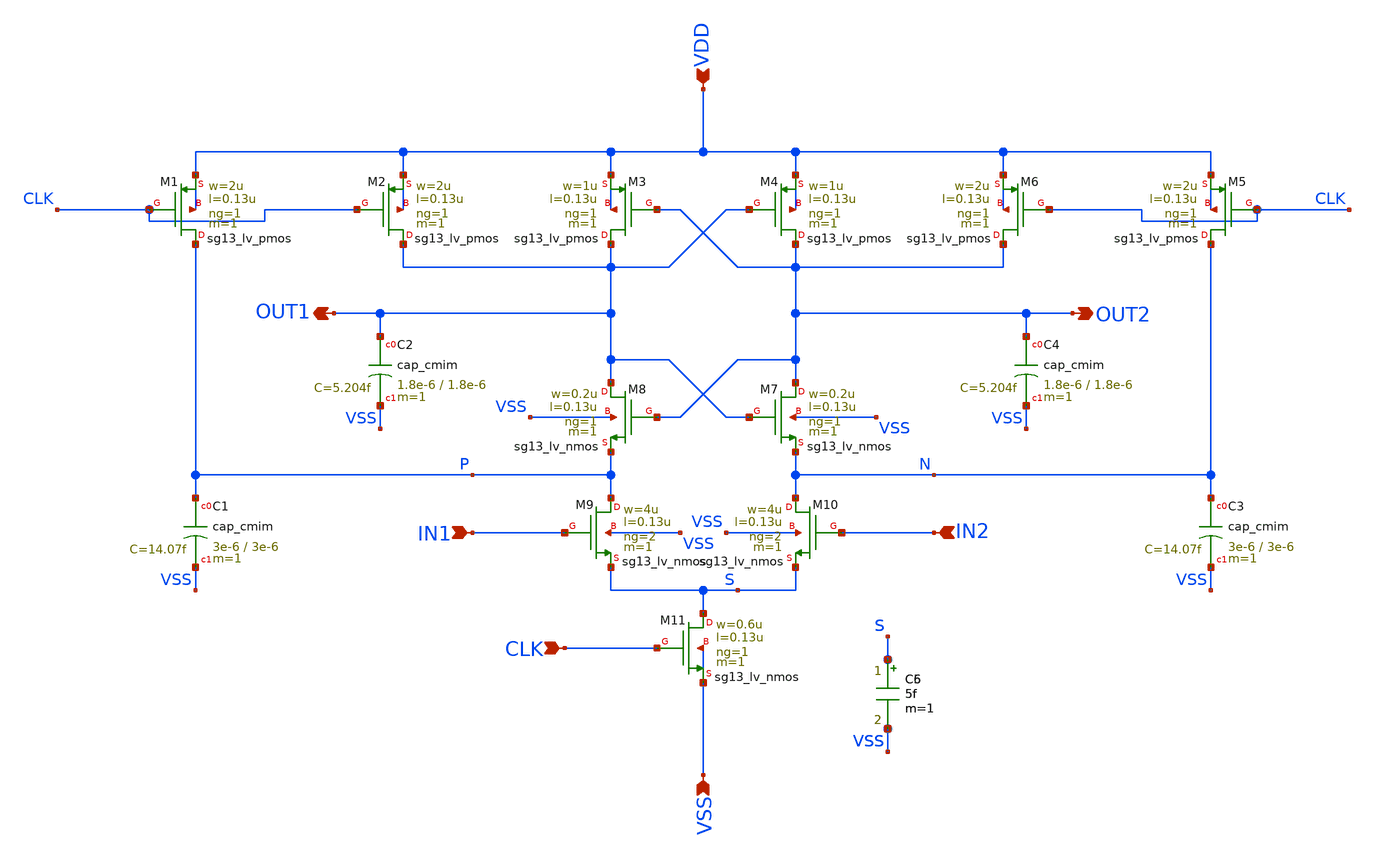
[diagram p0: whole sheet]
** sch_path: designs/comparator_harald_test/comparator.sch
**.subckt comparator CLK IN1 IN2 OUT2 OUT1 VSS VDD
*.ipin CLK
*.ipin IN1
*.ipin IN2
*.opin OUT2
*.opin OUT1
*.ipin VSS
*.ipin VDD
XM1 P CLK VDD VDD sg13_lv_pmos w=2u l=0.13u ng=1 m=1 mm_ok=1
XM3 OUT1 OUT2 VDD VDD sg13_lv_pmos w=1u l=0.13u ng=1 m=1 mm_ok=1
XM4 OUT2 OUT1 VDD VDD sg13_lv_pmos w=1u l=0.13u ng=1 m=1 mm_ok=1
XM8 OUT1 OUT2 P VSS sg13_lv_nmos w=0.2u l=0.13u ng=1 m=1 mm_ok=1
XM9 P IN1 S VSS sg13_lv_nmos w=4u l=0.13u ng=2 m=1 mm_ok=1
XM11 S CLK VSS VSS sg13_lv_nmos w=0.6u l=0.13u ng=1 m=1 mm_ok=1
XM10 N IN2 S VSS sg13_lv_nmos w=4u l=0.13u ng=2 m=1 mm_ok=1
XM2 OUT1 CLK VDD VDD sg13_lv_pmos w=2u l=0.13u ng=1 m=1 mm_ok=1
XM5 N CLK VDD VDD sg13_lv_pmos w=2u l=0.13u ng=1 m=1 mm_ok=1
XM6 OUT2 CLK VDD VDD sg13_lv_pmos w=2u l=0.13u ng=1 m=1 mm_ok=1
XM7 OUT2 OUT1 N VSS sg13_lv_nmos w=0.2u l=0.13u ng=1 m=1 mm_ok=1
XC2 OUT1 VSS cap_cmim w=1.8e-6 l=1.8e-6 m=1 mm_ok=1
XC4 OUT2 VSS cap_cmim w=1.8e-6 l=1.8e-6 m=1 mm_ok=1
XC1 P VSS cap_cmim w=3e-6 l=3e-6 m=1 mm_ok=1
XC3 N VSS cap_cmim w=3e-6 l=3e-6 m=1 mm_ok=1
C5 S VSS 5f m=1
C6 S VSS 5f m=1
**.ends
.end
